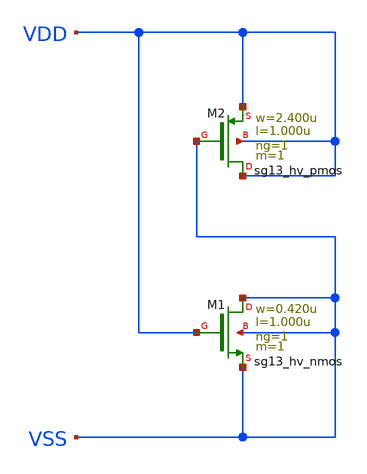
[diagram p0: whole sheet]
** sch_path: ihp-sg13g2/libs.ref/sg13g2_stdcell_hv/sch/xschem/sg13g2_hv_decap_4.sch
* Copyright 2023 IHP PDK Authors
* Licensed under the Apache License, Version 2.0 (the "License");
* you may not use this file except in compliance with the License.
* You may obtain a copy of the License at
* https://www.apache.org/licenses/LICENSE-2.0
* Unless required by applicable law or agreed to in writing, software
* distributed under the License is distributed on an "AS IS" BASIS,
* WITHOUT WARRANTIES OR CONDITIONS OF ANY KIND, either express or implied.
* See the License for the specific language governing permissions and
* limitations under the License.
**.subckt sg13g2_hv_decap_4
XM1 VSS VDD VSS VSS sg13_hv_nmos w=0.420u l=1.000u ng=1 m=1 mm_ok=1
XM2 VDD VSS VDD VDD sg13_hv_pmos w=2.400u l=1.000u ng=1 m=1 mm_ok=1
**.ends
.end
